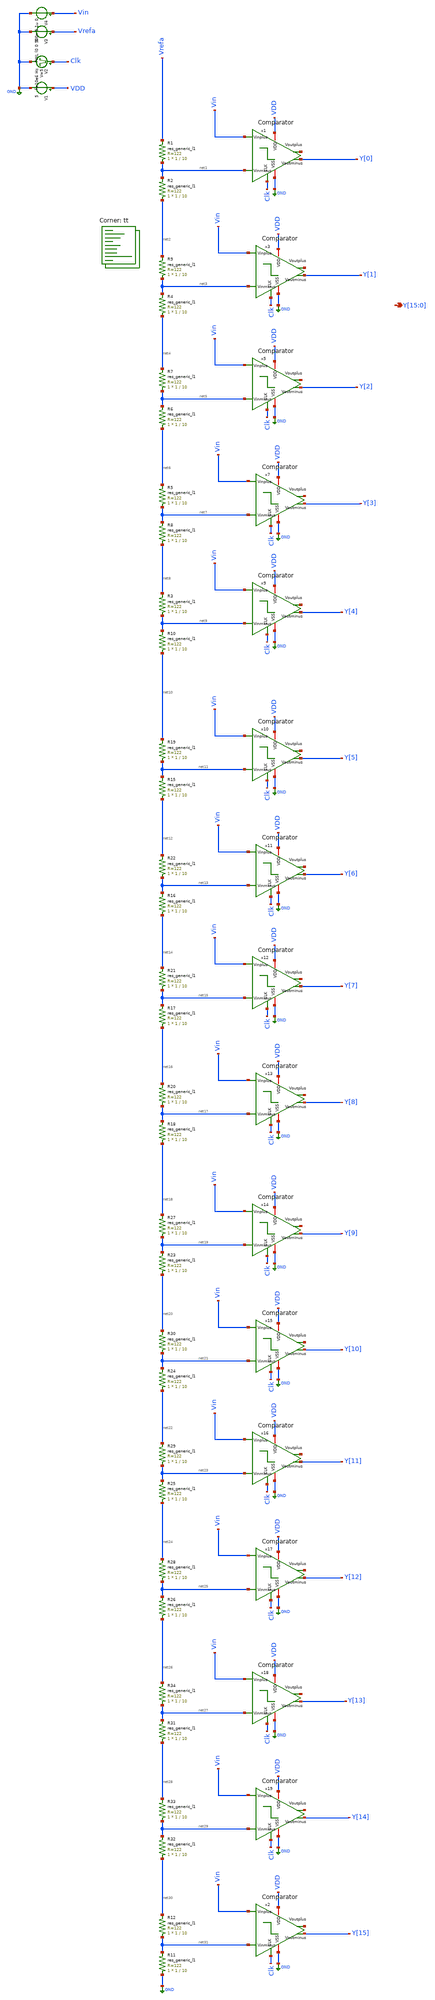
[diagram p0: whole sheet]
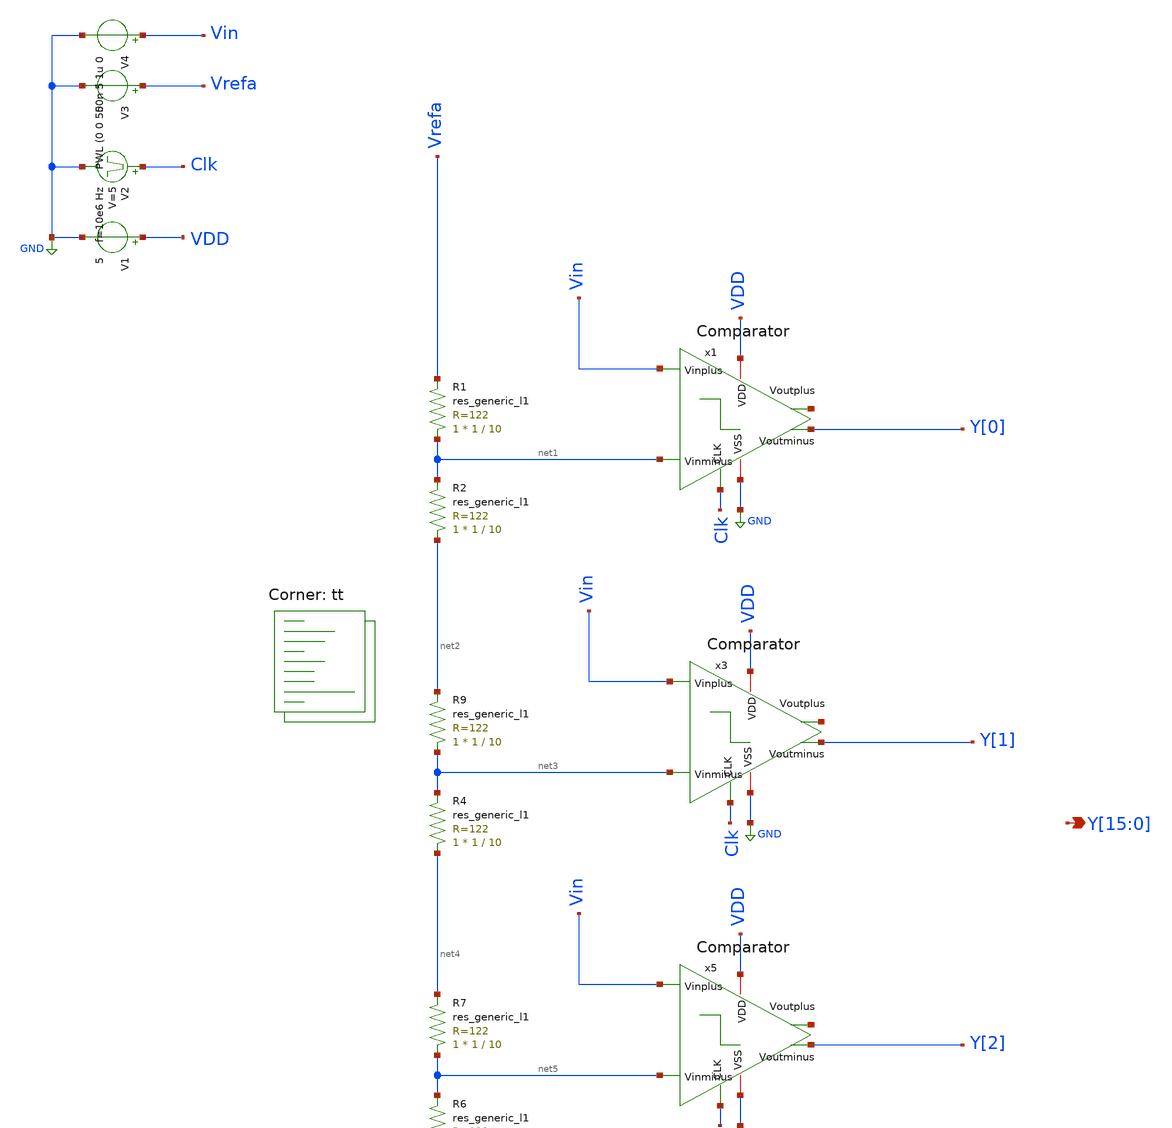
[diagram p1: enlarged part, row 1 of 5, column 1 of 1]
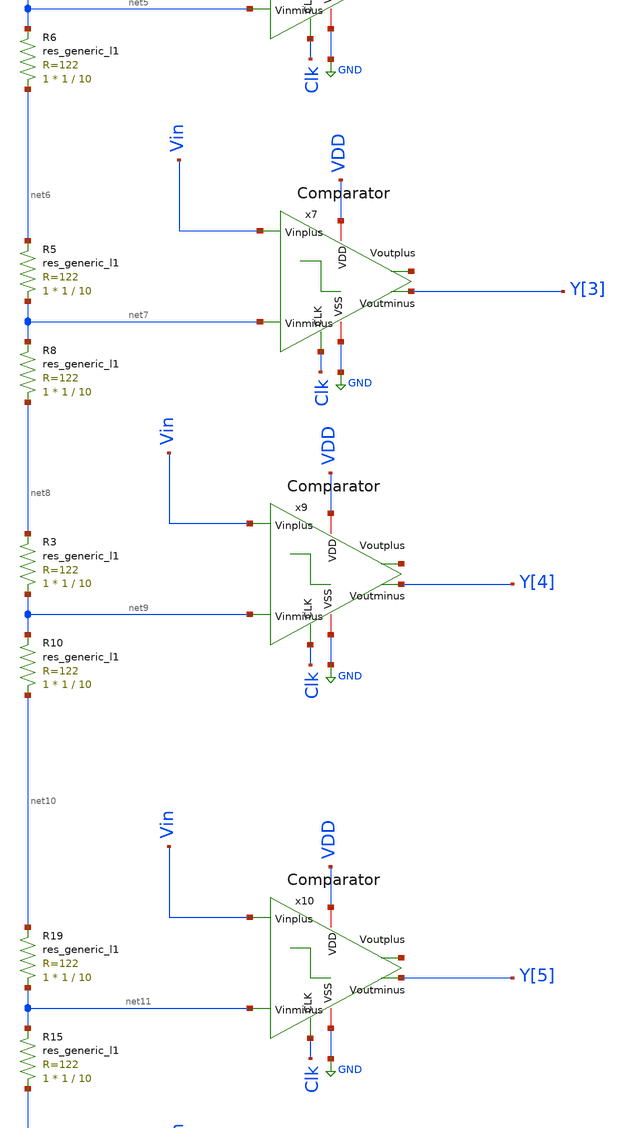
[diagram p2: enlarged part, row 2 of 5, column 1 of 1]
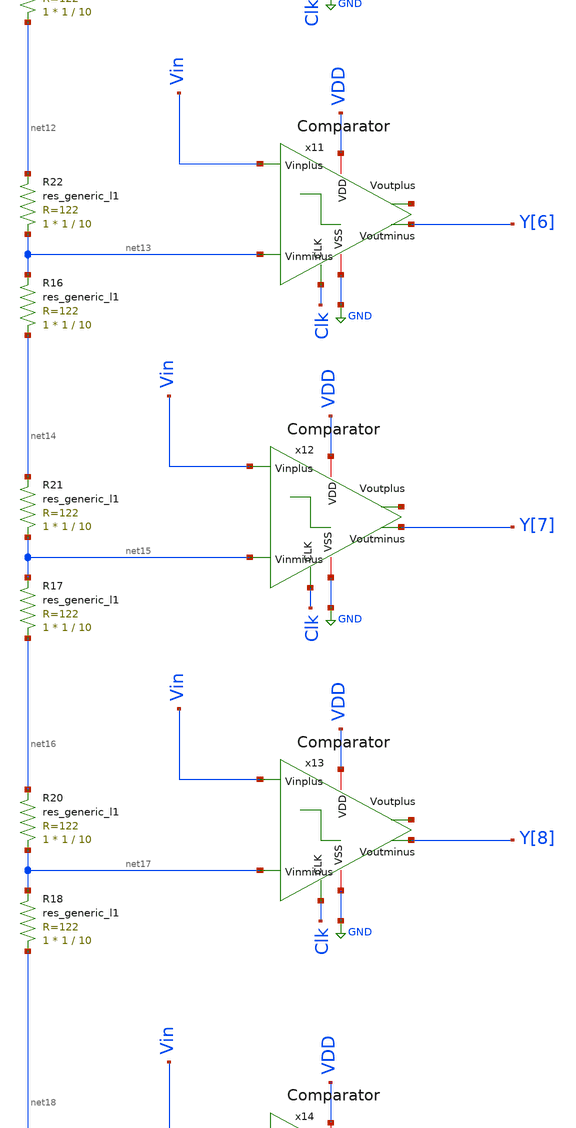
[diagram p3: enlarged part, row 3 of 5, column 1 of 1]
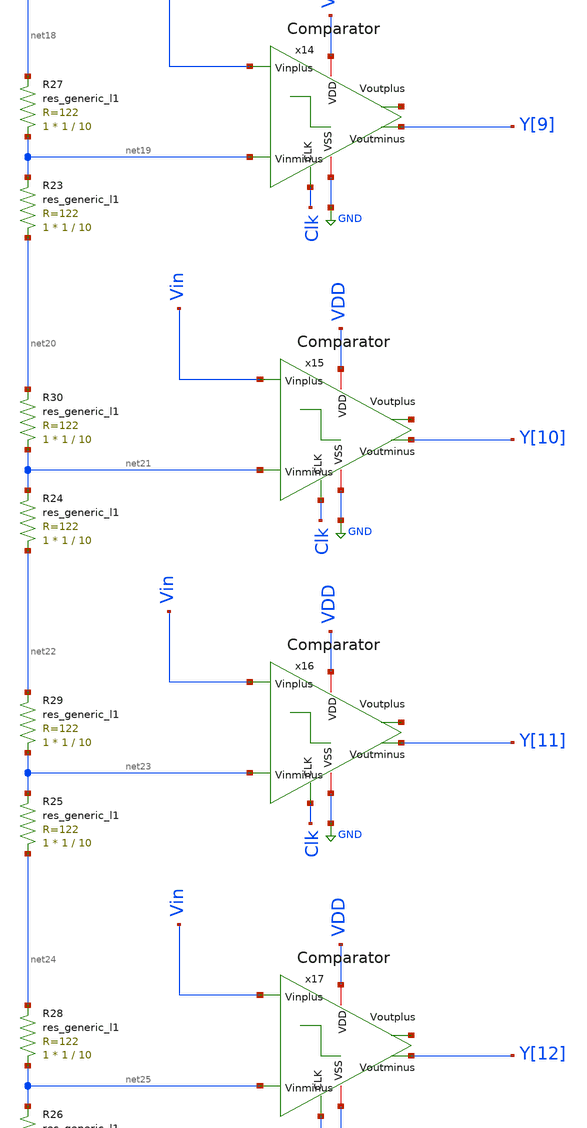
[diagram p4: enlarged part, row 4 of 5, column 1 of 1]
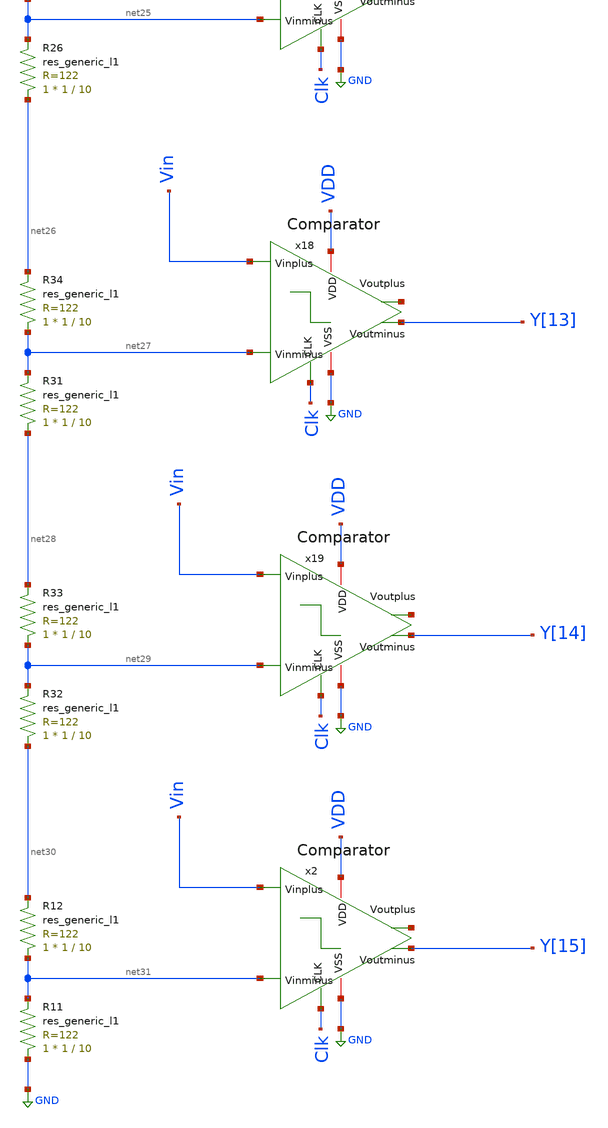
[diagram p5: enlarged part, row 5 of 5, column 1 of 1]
** sch_path: xschem/Amplifiers/4bitADC.sch
**.subckt 4bitADC
*+ Y[15],Y[14],Y[13],Y[12],Y[11],Y[10],Y[9],Y[8],Y[7],Y[6],Y[5],Y[4],Y[3],Y[2],Y[1],Y[0]
*.opin Y[15],Y[14],Y[13],Y[12],Y[11],Y[10],Y[9],Y[8],Y[7],Y[6],Y[5],Y[4],Y[3],Y[2],Y[1],Y[0]
R2 net2 net1 sky130_fd_pr__res_generic_l1 W=1 L=10 m=1
x1 VDD Y[0] net32 Clk Vin net1 GND Comparator
R4 net4 net3 sky130_fd_pr__res_generic_l1 W=1 L=10 m=1
R6 net6 net5 sky130_fd_pr__res_generic_l1 W=1 L=10 m=1
R8 net8 net7 sky130_fd_pr__res_generic_l1 W=1 L=10 m=1
R10 net10 net9 sky130_fd_pr__res_generic_l1 W=1 L=10 m=1
V1 VDD GND 5
V3 Vrefa GND 5
V4 Vin GND PWL (0 0 500n 5 1u 0
x3 VDD Y[1] net33 Clk Vin net3 GND Comparator
x5 VDD Y[2] net34 Clk Vin net5 GND Comparator
x7 VDD Y[3] net35 Clk Vin net7 GND Comparator
x9 VDD Y[4] net36 Clk Vin net9 GND Comparator
V2 Clk GND pulse 0 5 '0.495/ 10e6 ' '0.01/10e6 ' '0.01/10e6 ' '0.49/10e6 ' '1/10e6 '
R1 net1 Vrefa sky130_fd_pr__res_generic_l1 W=1 L=10 m=1
R3 net9 net8 sky130_fd_pr__res_generic_l1 W=1 L=10 m=1
R5 net7 net6 sky130_fd_pr__res_generic_l1 W=1 L=10 m=1
R7 net5 net4 sky130_fd_pr__res_generic_l1 W=1 L=10 m=1
R9 net3 net2 sky130_fd_pr__res_generic_l1 W=1 L=10 m=1
R15 net12 net11 sky130_fd_pr__res_generic_l1 W=1 L=10 m=1
x10 VDD Y[5] net37 Clk Vin net11 GND Comparator
R16 net14 net13 sky130_fd_pr__res_generic_l1 W=1 L=10 m=1
R17 net16 net15 sky130_fd_pr__res_generic_l1 W=1 L=10 m=1
R18 net18 net17 sky130_fd_pr__res_generic_l1 W=1 L=10 m=1
x11 VDD Y[6] net38 Clk Vin net13 GND Comparator
x12 VDD Y[7] net39 Clk Vin net15 GND Comparator
x13 VDD Y[8] net40 Clk Vin net17 GND Comparator
R19 net11 net10 sky130_fd_pr__res_generic_l1 W=1 L=10 m=1
R20 net17 net16 sky130_fd_pr__res_generic_l1 W=1 L=10 m=1
R21 net15 net14 sky130_fd_pr__res_generic_l1 W=1 L=10 m=1
R22 net13 net12 sky130_fd_pr__res_generic_l1 W=1 L=10 m=1
R23 net20 net19 sky130_fd_pr__res_generic_l1 W=1 L=10 m=1
x14 VDD Y[9] net41 Clk Vin net19 GND Comparator
R24 net22 net21 sky130_fd_pr__res_generic_l1 W=1 L=10 m=1
R25 net24 net23 sky130_fd_pr__res_generic_l1 W=1 L=10 m=1
R26 net26 net25 sky130_fd_pr__res_generic_l1 W=1 L=10 m=1
x15 VDD Y[10] net42 Clk Vin net21 GND Comparator
x16 VDD Y[11] net43 Clk Vin net23 GND Comparator
x17 VDD Y[12] net44 Clk Vin net25 GND Comparator
R27 net19 net18 sky130_fd_pr__res_generic_l1 W=1 L=10 m=1
R28 net25 net24 sky130_fd_pr__res_generic_l1 W=1 L=10 m=1
R29 net23 net22 sky130_fd_pr__res_generic_l1 W=1 L=10 m=1
R30 net21 net20 sky130_fd_pr__res_generic_l1 W=1 L=10 m=1
R31 net28 net27 sky130_fd_pr__res_generic_l1 W=1 L=10 m=1
R32 net30 net29 sky130_fd_pr__res_generic_l1 W=1 L=10 m=1
x18 VDD Y[13] net45 Clk Vin net27 GND Comparator
x19 VDD Y[14] net46 Clk Vin net29 GND Comparator
R33 net29 net28 sky130_fd_pr__res_generic_l1 W=1 L=10 m=1
R34 net27 net26 sky130_fd_pr__res_generic_l1 W=1 L=10 m=1
R11 GND net31 sky130_fd_pr__res_generic_l1 W=1 L=10 m=1
x2 VDD Y[15] net47 Clk Vin net31 GND Comparator
R12 net31 net30 sky130_fd_pr__res_generic_l1 W=1 L=10 m=1
**** begin user architecture code
.lib $::SKYWATER_MODELS/sky130.lib.spice tt


.op
.tran 100n 1u
.save all



** opencircuitdesign pdks install
.lib $::SKYWATER_MODELS/sky130.lib.spice tt


**** end user architecture code
**.ends
.GLOBAL GND
.end
